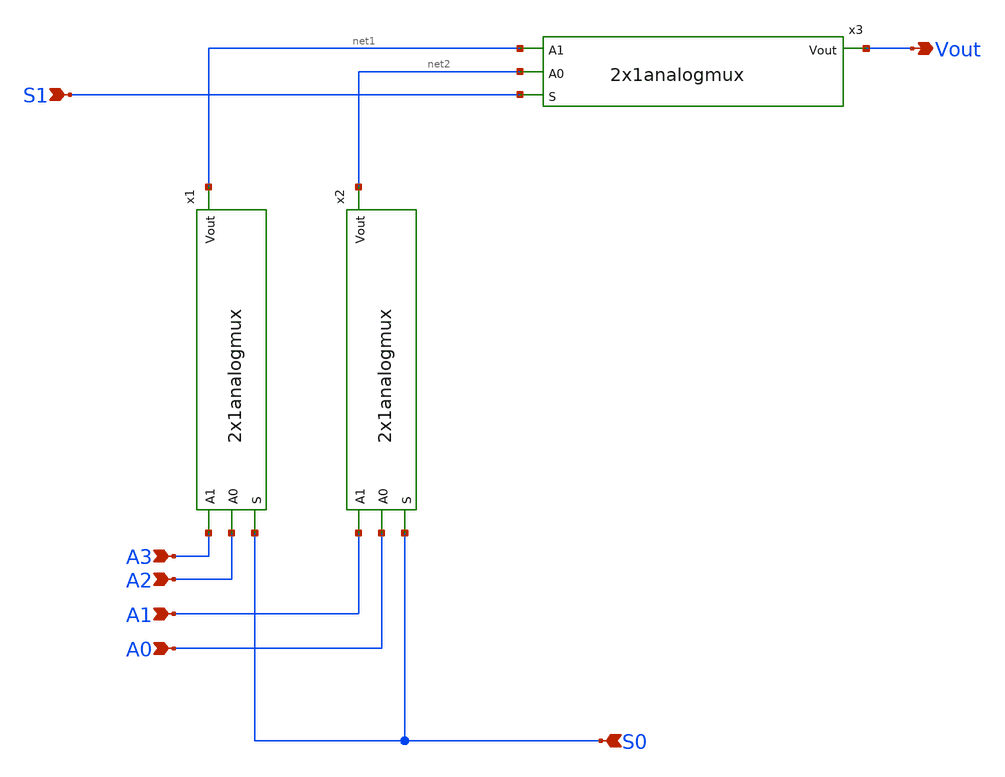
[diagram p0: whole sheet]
** sch_path: 4x1analogmux.sch
* 2x1analogmux.sch:
* Copyright 2021 Stefan Frederik Schippers
* Licensed under the Apache License, Version 2.0 (the "License");
**.subckt 4x1analogmux A3 A2 A1 A0 S1 S0 Vout
*.ipin A3
*.ipin A2
*.ipin A1
*.ipin A0
*.ipin S1
*.ipin S0
*.opin Vout
x2 net2 A1 A0 S0 2x1analogmux
x3 Vout net1 net2 S1 2x1analogmux
x1 net1 A3 A2 S0 2x1analogmux
**.ends

* expanding   symbol:  symbols/2x1analogmux.sym # of pins=4
** sym_path: 2x1analogmux.sym
** sch_path: 2x1analogmux.sch
.subckt 2x1analogmux Vout A1 A0 S
*.ipin S
*.opin Vout
*.ipin A1
*.ipin A0
x1 net1 A1 Vout S dacpassgate
x2 S A0 Vout net1 dacpassgate
x4 net1 S VDD GND not W_N=1 L_N=0.15 W_P=2 L_P=0.15 m=10
.ends


* expanding   symbol:  symbols/dacpassgate.sym # of pins=4
** sym_path: dacpassgate.sym
** sch_path: dacpassgate.sch
.subckt dacpassgate GP A Z GN
*.iopin A
*.iopin Z
*.ipin GP
*.ipin GN
XM1 Z GN A GND sky130_fd_pr__nfet_01v8 L=0.5 W=1 nf=1 ad='int((nf+1)/2) * W/nf * 0.29' as='int((nf+2)/2) * W/nf * 0.29'
+ pd='2*int((nf+1)/2) * (W/nf + 0.29)' ps='2*int((nf+2)/2) * (W/nf + 0.29)' nrd='0.29 / W' nrs='0.29 / W'
+ sa=0 sb=0 sd=0 mult=10 m=10
XM2 Z GP A VDD sky130_fd_pr__pfet_01v8 L=0.5 W=2 nf=1 ad='int((nf+1)/2) * W/nf * 0.29' as='int((nf+2)/2) * W/nf * 0.29'
+ pd='2*int((nf+1)/2) * (W/nf + 0.29)' ps='2*int((nf+2)/2) * (W/nf + 0.29)' nrd='0.29 / W' nrs='0.29 / W'
+ sa=0 sb=0 sd=0 mult=10 m=10
.ends


* expanding   symbol:  symbols/not.sym # of pins=2
** sym_path: symbols/not.sym
** sch_path: symbols/not.sch
.subckt not y a VCCPIN VSSPIN     W_N=1 L_N=0.15 W_P=2 L_P=0.15
*.opin y
*.ipin a
XM1 DN a VSSPIN VSSPIN sky130_fd_pr__nfet_01v8 L=L_N W=W_N nf=1 ad='int((1 + 1)/2) * W_N / 1 * 0.29'
+ as='int((1 + 2)/2) * W_N / 1 * 0.29' pd='2*int((1 + 1)/2) * (W_N / 1 + 0.29)' ps='2*int((1 + 2)/2) * (W_N / 1 + 0.29)'
+ nrd='0.29 / W_N ' nrs='0.29 / W_N ' sa=0 sb=0 sd=0 mult=1 m=1
XM2 DP a VCCPIN VCCPIN sky130_fd_pr__pfet_01v8 L=L_P W=W_P nf=1 ad='int((nf+1)/2) * W/nf * 0.29' as='int((nf+2)/2) * W/nf * 0.29'
+ pd='2*int((nf+1)/2) * (W/nf + 0.29)' ps='2*int((nf+2)/2) * (W/nf + 0.29)' nrd='0.29 / W' nrs='0.29 / W'
+ sa=0 sb=0 sd=0 mult=1 m=1
Vmeas DP y 0
.save i(vmeas)
Vmeas1 y DN 0
.save i(vmeas1)
.save v(dp)
.save v(dn)
.ends

.end
